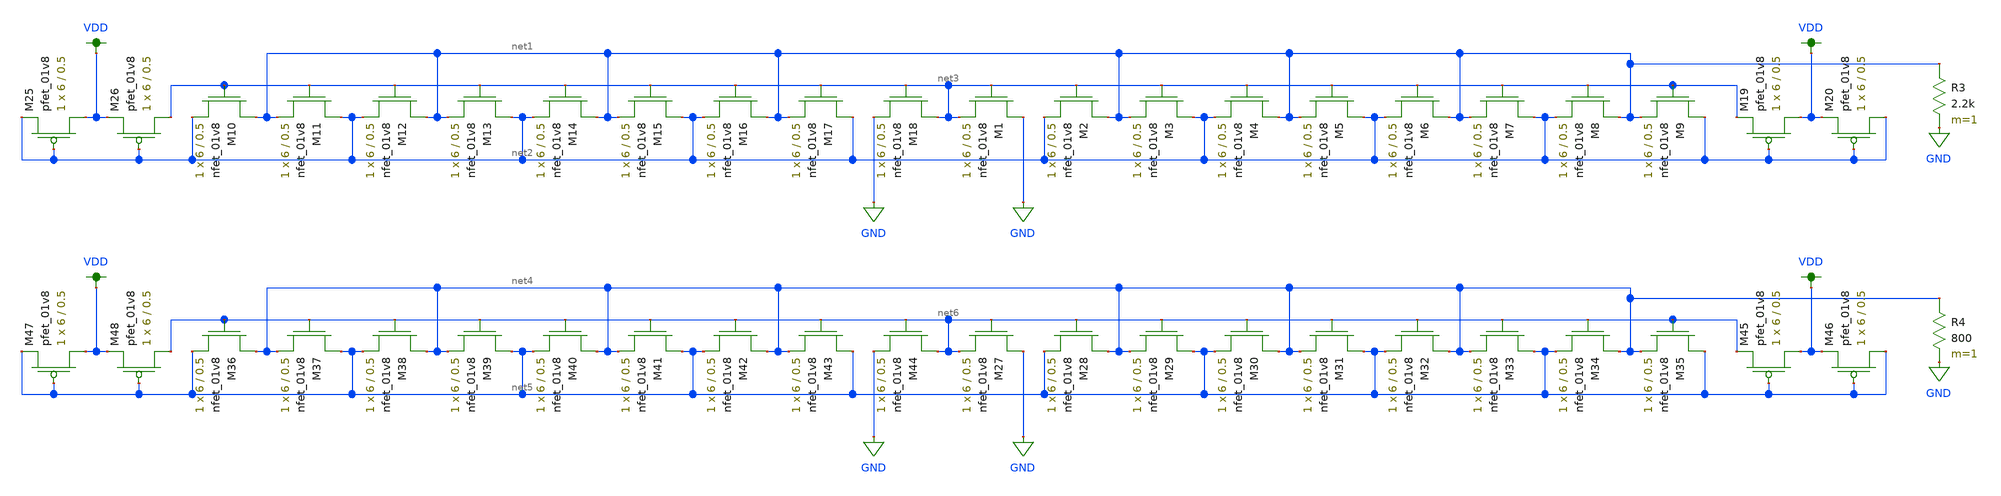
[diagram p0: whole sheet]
** sch_path: schematics/bias_lds.sch
**.subckt bias_lds
XM1 GND net3 net3 GND sky130_fd_pr__nfet_01v8 L=0.5 W=6 nf=1 ad='int((nf+1)/2) * W/nf * 0.29' as='int((nf+2)/2) * W/nf * 0.29'
+ pd='2*int((nf+1)/2) * (W/nf + 0.29)' ps='2*int((nf+2)/2) * (W/nf + 0.29)' nrd='0.29 / W' nrs='0.29 / W'
+ sa=0 sb=0 sd=0 mult=1 m=1
XM2 net1 net3 net2 GND sky130_fd_pr__nfet_01v8 L=0.5 W=6 nf=1 ad='int((nf+1)/2) * W/nf * 0.29' as='int((nf+2)/2) * W/nf * 0.29'
+ pd='2*int((nf+1)/2) * (W/nf + 0.29)' ps='2*int((nf+2)/2) * (W/nf + 0.29)' nrd='0.29 / W' nrs='0.29 / W'
+ sa=0 sb=0 sd=0 mult=1 m=1
XM3 net2 net3 net1 GND sky130_fd_pr__nfet_01v8 L=0.5 W=6 nf=1 ad='int((nf+1)/2) * W/nf * 0.29' as='int((nf+2)/2) * W/nf * 0.29'
+ pd='2*int((nf+1)/2) * (W/nf + 0.29)' ps='2*int((nf+2)/2) * (W/nf + 0.29)' nrd='0.29 / W' nrs='0.29 / W'
+ sa=0 sb=0 sd=0 mult=1 m=1
XM4 net1 net3 net2 GND sky130_fd_pr__nfet_01v8 L=0.5 W=6 nf=1 ad='int((nf+1)/2) * W/nf * 0.29' as='int((nf+2)/2) * W/nf * 0.29'
+ pd='2*int((nf+1)/2) * (W/nf + 0.29)' ps='2*int((nf+2)/2) * (W/nf + 0.29)' nrd='0.29 / W' nrs='0.29 / W'
+ sa=0 sb=0 sd=0 mult=1 m=1
XM5 net2 net3 net1 GND sky130_fd_pr__nfet_01v8 L=0.5 W=6 nf=1 ad='int((nf+1)/2) * W/nf * 0.29' as='int((nf+2)/2) * W/nf * 0.29'
+ pd='2*int((nf+1)/2) * (W/nf + 0.29)' ps='2*int((nf+2)/2) * (W/nf + 0.29)' nrd='0.29 / W' nrs='0.29 / W'
+ sa=0 sb=0 sd=0 mult=1 m=1
XM6 net1 net3 net2 GND sky130_fd_pr__nfet_01v8 L=0.5 W=6 nf=1 ad='int((nf+1)/2) * W/nf * 0.29' as='int((nf+2)/2) * W/nf * 0.29'
+ pd='2*int((nf+1)/2) * (W/nf + 0.29)' ps='2*int((nf+2)/2) * (W/nf + 0.29)' nrd='0.29 / W' nrs='0.29 / W'
+ sa=0 sb=0 sd=0 mult=1 m=1
XM7 net2 net3 net1 GND sky130_fd_pr__nfet_01v8 L=0.5 W=6 nf=1 ad='int((nf+1)/2) * W/nf * 0.29' as='int((nf+2)/2) * W/nf * 0.29'
+ pd='2*int((nf+1)/2) * (W/nf + 0.29)' ps='2*int((nf+2)/2) * (W/nf + 0.29)' nrd='0.29 / W' nrs='0.29 / W'
+ sa=0 sb=0 sd=0 mult=1 m=1
XM8 net1 net3 net2 GND sky130_fd_pr__nfet_01v8 L=0.5 W=6 nf=1 ad='int((nf+1)/2) * W/nf * 0.29' as='int((nf+2)/2) * W/nf * 0.29'
+ pd='2*int((nf+1)/2) * (W/nf + 0.29)' ps='2*int((nf+2)/2) * (W/nf + 0.29)' nrd='0.29 / W' nrs='0.29 / W'
+ sa=0 sb=0 sd=0 mult=1 m=1
XM9 net2 net3 net1 GND sky130_fd_pr__nfet_01v8 L=0.5 W=6 nf=1 ad='int((nf+1)/2) * W/nf * 0.29' as='int((nf+2)/2) * W/nf * 0.29'
+ pd='2*int((nf+1)/2) * (W/nf + 0.29)' ps='2*int((nf+2)/2) * (W/nf + 0.29)' nrd='0.29 / W' nrs='0.29 / W'
+ sa=0 sb=0 sd=0 mult=1 m=1
XM10 net1 net3 net2 GND sky130_fd_pr__nfet_01v8 L=0.5 W=6 nf=1 ad='int((nf+1)/2) * W/nf * 0.29' as='int((nf+2)/2) * W/nf * 0.29'
+ pd='2*int((nf+1)/2) * (W/nf + 0.29)' ps='2*int((nf+2)/2) * (W/nf + 0.29)' nrd='0.29 / W' nrs='0.29 / W'
+ sa=0 sb=0 sd=0 mult=1 m=1
XM11 net2 net3 net1 GND sky130_fd_pr__nfet_01v8 L=0.5 W=6 nf=1 ad='int((nf+1)/2) * W/nf * 0.29' as='int((nf+2)/2) * W/nf * 0.29'
+ pd='2*int((nf+1)/2) * (W/nf + 0.29)' ps='2*int((nf+2)/2) * (W/nf + 0.29)' nrd='0.29 / W' nrs='0.29 / W'
+ sa=0 sb=0 sd=0 mult=1 m=1
XM12 net1 net3 net2 GND sky130_fd_pr__nfet_01v8 L=0.5 W=6 nf=1 ad='int((nf+1)/2) * W/nf * 0.29' as='int((nf+2)/2) * W/nf * 0.29'
+ pd='2*int((nf+1)/2) * (W/nf + 0.29)' ps='2*int((nf+2)/2) * (W/nf + 0.29)' nrd='0.29 / W' nrs='0.29 / W'
+ sa=0 sb=0 sd=0 mult=1 m=1
XM13 net2 net3 net1 GND sky130_fd_pr__nfet_01v8 L=0.5 W=6 nf=1 ad='int((nf+1)/2) * W/nf * 0.29' as='int((nf+2)/2) * W/nf * 0.29'
+ pd='2*int((nf+1)/2) * (W/nf + 0.29)' ps='2*int((nf+2)/2) * (W/nf + 0.29)' nrd='0.29 / W' nrs='0.29 / W'
+ sa=0 sb=0 sd=0 mult=1 m=1
XM14 net1 net3 net2 GND sky130_fd_pr__nfet_01v8 L=0.5 W=6 nf=1 ad='int((nf+1)/2) * W/nf * 0.29' as='int((nf+2)/2) * W/nf * 0.29'
+ pd='2*int((nf+1)/2) * (W/nf + 0.29)' ps='2*int((nf+2)/2) * (W/nf + 0.29)' nrd='0.29 / W' nrs='0.29 / W'
+ sa=0 sb=0 sd=0 mult=1 m=1
XM15 net2 net3 net1 GND sky130_fd_pr__nfet_01v8 L=0.5 W=6 nf=1 ad='int((nf+1)/2) * W/nf * 0.29' as='int((nf+2)/2) * W/nf * 0.29'
+ pd='2*int((nf+1)/2) * (W/nf + 0.29)' ps='2*int((nf+2)/2) * (W/nf + 0.29)' nrd='0.29 / W' nrs='0.29 / W'
+ sa=0 sb=0 sd=0 mult=1 m=1
XM16 net1 net3 net2 GND sky130_fd_pr__nfet_01v8 L=0.5 W=6 nf=1 ad='int((nf+1)/2) * W/nf * 0.29' as='int((nf+2)/2) * W/nf * 0.29'
+ pd='2*int((nf+1)/2) * (W/nf + 0.29)' ps='2*int((nf+2)/2) * (W/nf + 0.29)' nrd='0.29 / W' nrs='0.29 / W'
+ sa=0 sb=0 sd=0 mult=1 m=1
XM17 net2 net3 net1 GND sky130_fd_pr__nfet_01v8 L=0.5 W=6 nf=1 ad='int((nf+1)/2) * W/nf * 0.29' as='int((nf+2)/2) * W/nf * 0.29'
+ pd='2*int((nf+1)/2) * (W/nf + 0.29)' ps='2*int((nf+2)/2) * (W/nf + 0.29)' nrd='0.29 / W' nrs='0.29 / W'
+ sa=0 sb=0 sd=0 mult=1 m=1
XM18 net3 net3 GND GND sky130_fd_pr__nfet_01v8 L=0.5 W=6 nf=1 ad='int((nf+1)/2) * W/nf * 0.29' as='int((nf+2)/2) * W/nf * 0.29'
+ pd='2*int((nf+1)/2) * (W/nf + 0.29)' ps='2*int((nf+2)/2) * (W/nf + 0.29)' nrd='0.29 / W' nrs='0.29 / W'
+ sa=0 sb=0 sd=0 mult=1 m=1
XM19 VDD net2 net3 VDD sky130_fd_pr__pfet_01v8 L=0.5 W=6 nf=1 ad='int((nf+1)/2) * W/nf * 0.29' as='int((nf+2)/2) * W/nf * 0.29'
+ pd='2*int((nf+1)/2) * (W/nf + 0.29)' ps='2*int((nf+2)/2) * (W/nf + 0.29)' nrd='0.29 / W' nrs='0.29 / W'
+ sa=0 sb=0 sd=0 mult=1 m=1
XM20 net2 net2 VDD VDD sky130_fd_pr__pfet_01v8 L=0.5 W=6 nf=1 ad='int((nf+1)/2) * W/nf * 0.29' as='int((nf+2)/2) * W/nf * 0.29'
+ pd='2*int((nf+1)/2) * (W/nf + 0.29)' ps='2*int((nf+2)/2) * (W/nf + 0.29)' nrd='0.29 / W' nrs='0.29 / W'
+ sa=0 sb=0 sd=0 mult=1 m=1
XM25 VDD net2 net2 VDD sky130_fd_pr__pfet_01v8 L=0.5 W=6 nf=1 ad='int((nf+1)/2) * W/nf * 0.29' as='int((nf+2)/2) * W/nf * 0.29'
+ pd='2*int((nf+1)/2) * (W/nf + 0.29)' ps='2*int((nf+2)/2) * (W/nf + 0.29)' nrd='0.29 / W' nrs='0.29 / W'
+ sa=0 sb=0 sd=0 mult=1 m=1
XM26 net3 net2 VDD VDD sky130_fd_pr__pfet_01v8 L=0.5 W=6 nf=1 ad='int((nf+1)/2) * W/nf * 0.29' as='int((nf+2)/2) * W/nf * 0.29'
+ pd='2*int((nf+1)/2) * (W/nf + 0.29)' ps='2*int((nf+2)/2) * (W/nf + 0.29)' nrd='0.29 / W' nrs='0.29 / W'
+ sa=0 sb=0 sd=0 mult=1 m=1
R3 net1 GND 2.2k m=1
XM27 GND net6 net6 GND sky130_fd_pr__nfet_01v8 L=0.5 W=6 nf=1 ad='int((nf+1)/2) * W/nf * 0.29' as='int((nf+2)/2) * W/nf * 0.29'
+ pd='2*int((nf+1)/2) * (W/nf + 0.29)' ps='2*int((nf+2)/2) * (W/nf + 0.29)' nrd='0.29 / W' nrs='0.29 / W'
+ sa=0 sb=0 sd=0 mult=1 m=1
XM28 net4 net6 net5 GND sky130_fd_pr__nfet_01v8 L=0.5 W=6 nf=1 ad='int((nf+1)/2) * W/nf * 0.29' as='int((nf+2)/2) * W/nf * 0.29'
+ pd='2*int((nf+1)/2) * (W/nf + 0.29)' ps='2*int((nf+2)/2) * (W/nf + 0.29)' nrd='0.29 / W' nrs='0.29 / W'
+ sa=0 sb=0 sd=0 mult=1 m=1
XM29 net5 net6 net4 GND sky130_fd_pr__nfet_01v8 L=0.5 W=6 nf=1 ad='int((nf+1)/2) * W/nf * 0.29' as='int((nf+2)/2) * W/nf * 0.29'
+ pd='2*int((nf+1)/2) * (W/nf + 0.29)' ps='2*int((nf+2)/2) * (W/nf + 0.29)' nrd='0.29 / W' nrs='0.29 / W'
+ sa=0 sb=0 sd=0 mult=1 m=1
XM30 net4 net6 net5 GND sky130_fd_pr__nfet_01v8 L=0.5 W=6 nf=1 ad='int((nf+1)/2) * W/nf * 0.29' as='int((nf+2)/2) * W/nf * 0.29'
+ pd='2*int((nf+1)/2) * (W/nf + 0.29)' ps='2*int((nf+2)/2) * (W/nf + 0.29)' nrd='0.29 / W' nrs='0.29 / W'
+ sa=0 sb=0 sd=0 mult=1 m=1
XM31 net5 net6 net4 GND sky130_fd_pr__nfet_01v8 L=0.5 W=6 nf=1 ad='int((nf+1)/2) * W/nf * 0.29' as='int((nf+2)/2) * W/nf * 0.29'
+ pd='2*int((nf+1)/2) * (W/nf + 0.29)' ps='2*int((nf+2)/2) * (W/nf + 0.29)' nrd='0.29 / W' nrs='0.29 / W'
+ sa=0 sb=0 sd=0 mult=1 m=1
XM32 net4 net6 net5 GND sky130_fd_pr__nfet_01v8 L=0.5 W=6 nf=1 ad='int((nf+1)/2) * W/nf * 0.29' as='int((nf+2)/2) * W/nf * 0.29'
+ pd='2*int((nf+1)/2) * (W/nf + 0.29)' ps='2*int((nf+2)/2) * (W/nf + 0.29)' nrd='0.29 / W' nrs='0.29 / W'
+ sa=0 sb=0 sd=0 mult=1 m=1
XM33 net5 net6 net4 GND sky130_fd_pr__nfet_01v8 L=0.5 W=6 nf=1 ad='int((nf+1)/2) * W/nf * 0.29' as='int((nf+2)/2) * W/nf * 0.29'
+ pd='2*int((nf+1)/2) * (W/nf + 0.29)' ps='2*int((nf+2)/2) * (W/nf + 0.29)' nrd='0.29 / W' nrs='0.29 / W'
+ sa=0 sb=0 sd=0 mult=1 m=1
XM34 net4 net6 net5 GND sky130_fd_pr__nfet_01v8 L=0.5 W=6 nf=1 ad='int((nf+1)/2) * W/nf * 0.29' as='int((nf+2)/2) * W/nf * 0.29'
+ pd='2*int((nf+1)/2) * (W/nf + 0.29)' ps='2*int((nf+2)/2) * (W/nf + 0.29)' nrd='0.29 / W' nrs='0.29 / W'
+ sa=0 sb=0 sd=0 mult=1 m=1
XM35 net5 net6 net4 GND sky130_fd_pr__nfet_01v8 L=0.5 W=6 nf=1 ad='int((nf+1)/2) * W/nf * 0.29' as='int((nf+2)/2) * W/nf * 0.29'
+ pd='2*int((nf+1)/2) * (W/nf + 0.29)' ps='2*int((nf+2)/2) * (W/nf + 0.29)' nrd='0.29 / W' nrs='0.29 / W'
+ sa=0 sb=0 sd=0 mult=1 m=1
XM36 net4 net6 net5 GND sky130_fd_pr__nfet_01v8 L=0.5 W=6 nf=1 ad='int((nf+1)/2) * W/nf * 0.29' as='int((nf+2)/2) * W/nf * 0.29'
+ pd='2*int((nf+1)/2) * (W/nf + 0.29)' ps='2*int((nf+2)/2) * (W/nf + 0.29)' nrd='0.29 / W' nrs='0.29 / W'
+ sa=0 sb=0 sd=0 mult=1 m=1
XM37 net5 net6 net4 GND sky130_fd_pr__nfet_01v8 L=0.5 W=6 nf=1 ad='int((nf+1)/2) * W/nf * 0.29' as='int((nf+2)/2) * W/nf * 0.29'
+ pd='2*int((nf+1)/2) * (W/nf + 0.29)' ps='2*int((nf+2)/2) * (W/nf + 0.29)' nrd='0.29 / W' nrs='0.29 / W'
+ sa=0 sb=0 sd=0 mult=1 m=1
XM38 net4 net6 net5 GND sky130_fd_pr__nfet_01v8 L=0.5 W=6 nf=1 ad='int((nf+1)/2) * W/nf * 0.29' as='int((nf+2)/2) * W/nf * 0.29'
+ pd='2*int((nf+1)/2) * (W/nf + 0.29)' ps='2*int((nf+2)/2) * (W/nf + 0.29)' nrd='0.29 / W' nrs='0.29 / W'
+ sa=0 sb=0 sd=0 mult=1 m=1
XM39 net5 net6 net4 GND sky130_fd_pr__nfet_01v8 L=0.5 W=6 nf=1 ad='int((nf+1)/2) * W/nf * 0.29' as='int((nf+2)/2) * W/nf * 0.29'
+ pd='2*int((nf+1)/2) * (W/nf + 0.29)' ps='2*int((nf+2)/2) * (W/nf + 0.29)' nrd='0.29 / W' nrs='0.29 / W'
+ sa=0 sb=0 sd=0 mult=1 m=1
XM40 net4 net6 net5 GND sky130_fd_pr__nfet_01v8 L=0.5 W=6 nf=1 ad='int((nf+1)/2) * W/nf * 0.29' as='int((nf+2)/2) * W/nf * 0.29'
+ pd='2*int((nf+1)/2) * (W/nf + 0.29)' ps='2*int((nf+2)/2) * (W/nf + 0.29)' nrd='0.29 / W' nrs='0.29 / W'
+ sa=0 sb=0 sd=0 mult=1 m=1
XM41 net5 net6 net4 GND sky130_fd_pr__nfet_01v8 L=0.5 W=6 nf=1 ad='int((nf+1)/2) * W/nf * 0.29' as='int((nf+2)/2) * W/nf * 0.29'
+ pd='2*int((nf+1)/2) * (W/nf + 0.29)' ps='2*int((nf+2)/2) * (W/nf + 0.29)' nrd='0.29 / W' nrs='0.29 / W'
+ sa=0 sb=0 sd=0 mult=1 m=1
XM42 net4 net6 net5 GND sky130_fd_pr__nfet_01v8 L=0.5 W=6 nf=1 ad='int((nf+1)/2) * W/nf * 0.29' as='int((nf+2)/2) * W/nf * 0.29'
+ pd='2*int((nf+1)/2) * (W/nf + 0.29)' ps='2*int((nf+2)/2) * (W/nf + 0.29)' nrd='0.29 / W' nrs='0.29 / W'
+ sa=0 sb=0 sd=0 mult=1 m=1
XM43 net5 net6 net4 GND sky130_fd_pr__nfet_01v8 L=0.5 W=6 nf=1 ad='int((nf+1)/2) * W/nf * 0.29' as='int((nf+2)/2) * W/nf * 0.29'
+ pd='2*int((nf+1)/2) * (W/nf + 0.29)' ps='2*int((nf+2)/2) * (W/nf + 0.29)' nrd='0.29 / W' nrs='0.29 / W'
+ sa=0 sb=0 sd=0 mult=1 m=1
XM44 net6 net6 GND GND sky130_fd_pr__nfet_01v8 L=0.5 W=6 nf=1 ad='int((nf+1)/2) * W/nf * 0.29' as='int((nf+2)/2) * W/nf * 0.29'
+ pd='2*int((nf+1)/2) * (W/nf + 0.29)' ps='2*int((nf+2)/2) * (W/nf + 0.29)' nrd='0.29 / W' nrs='0.29 / W'
+ sa=0 sb=0 sd=0 mult=1 m=1
XM45 VDD net5 net6 VDD sky130_fd_pr__pfet_01v8 L=0.5 W=6 nf=1 ad='int((nf+1)/2) * W/nf * 0.29' as='int((nf+2)/2) * W/nf * 0.29'
+ pd='2*int((nf+1)/2) * (W/nf + 0.29)' ps='2*int((nf+2)/2) * (W/nf + 0.29)' nrd='0.29 / W' nrs='0.29 / W'
+ sa=0 sb=0 sd=0 mult=1 m=1
XM46 net5 net5 VDD VDD sky130_fd_pr__pfet_01v8 L=0.5 W=6 nf=1 ad='int((nf+1)/2) * W/nf * 0.29' as='int((nf+2)/2) * W/nf * 0.29'
+ pd='2*int((nf+1)/2) * (W/nf + 0.29)' ps='2*int((nf+2)/2) * (W/nf + 0.29)' nrd='0.29 / W' nrs='0.29 / W'
+ sa=0 sb=0 sd=0 mult=1 m=1
XM47 VDD net5 net5 VDD sky130_fd_pr__pfet_01v8 L=0.5 W=6 nf=1 ad='int((nf+1)/2) * W/nf * 0.29' as='int((nf+2)/2) * W/nf * 0.29'
+ pd='2*int((nf+1)/2) * (W/nf + 0.29)' ps='2*int((nf+2)/2) * (W/nf + 0.29)' nrd='0.29 / W' nrs='0.29 / W'
+ sa=0 sb=0 sd=0 mult=1 m=1
XM48 net6 net5 VDD VDD sky130_fd_pr__pfet_01v8 L=0.5 W=6 nf=1 ad='int((nf+1)/2) * W/nf * 0.29' as='int((nf+2)/2) * W/nf * 0.29'
+ pd='2*int((nf+1)/2) * (W/nf + 0.29)' ps='2*int((nf+2)/2) * (W/nf + 0.29)' nrd='0.29 / W' nrs='0.29 / W'
+ sa=0 sb=0 sd=0 mult=1 m=1
R4 net4 GND 800 m=1
**.ends
.GLOBAL GND
.GLOBAL VDD
.end
